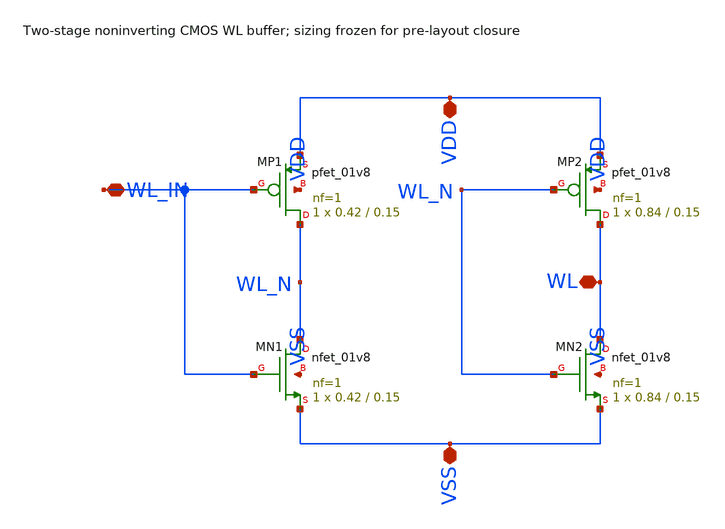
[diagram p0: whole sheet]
** sch_path: cells/wordline_driver/wl_driver.sch
**.subckt wl_driver VDD VSS WL_IN WL
*.iopin VDD
*.iopin VSS
*.iopin WL_IN
*.iopin WL
XMP1 WL_N WL_IN VDD VDD sky130_fd_pr__pfet_01v8 L=0.15 W=0.42 nf=1 ad='int((nf+1)/2) * W/nf * 0.29' as='int((nf+2)/2) * W/nf * 0.29'
+ pd='2*int((nf+1)/2) * (W/nf + 0.29)' ps='2*int((nf+2)/2) * (W/nf + 0.29)' nrd='0.29 / W' nrs='0.29 / W'
+ sa=0 sb=0 sd=0 mult=1 m=1
XMN1 WL_N WL_IN VSS VSS sky130_fd_pr__nfet_01v8 L=0.15 W=0.42 nf=1 ad='int((1 + 1)/2) * 0.42 / 1 * 0.29'
+ as='int((1 + 2)/2) * 0.42 / 1 * 0.29' pd='2*int((1 + 1)/2) * (0.42 / 1 + 0.29)' ps='2*int((1 + 2)/2) * (0.42 / 1 + 0.29)'
+ nrd='0.29 / 0.42 ' nrs='0.29 / 0.42 ' sa=0 sb=0 sd=0 mult=1 m=1
XMP2 WL WL_N VDD VDD sky130_fd_pr__pfet_01v8 L=0.15 W=0.84 nf=1 ad='int((nf+1)/2) * W/nf * 0.29' as='int((nf+2)/2) * W/nf * 0.29'
+ pd='2*int((nf+1)/2) * (W/nf + 0.29)' ps='2*int((nf+2)/2) * (W/nf + 0.29)' nrd='0.29 / W' nrs='0.29 / W'
+ sa=0 sb=0 sd=0 mult=1 m=1
XMN2 WL WL_N VSS VSS sky130_fd_pr__nfet_01v8 L=0.15 W=0.84 nf=1 ad='int((1 + 1)/2) * 0.84 / 1 * 0.29'
+ as='int((1 + 2)/2) * 0.84 / 1 * 0.29' pd='2*int((1 + 1)/2) * (0.84 / 1 + 0.29)' ps='2*int((1 + 2)/2) * (0.84 / 1 + 0.29)'
+ nrd='0.29 / 0.84 ' nrs='0.29 / 0.84 ' sa=0 sb=0 sd=0 mult=1 m=1
**.ends
.end
